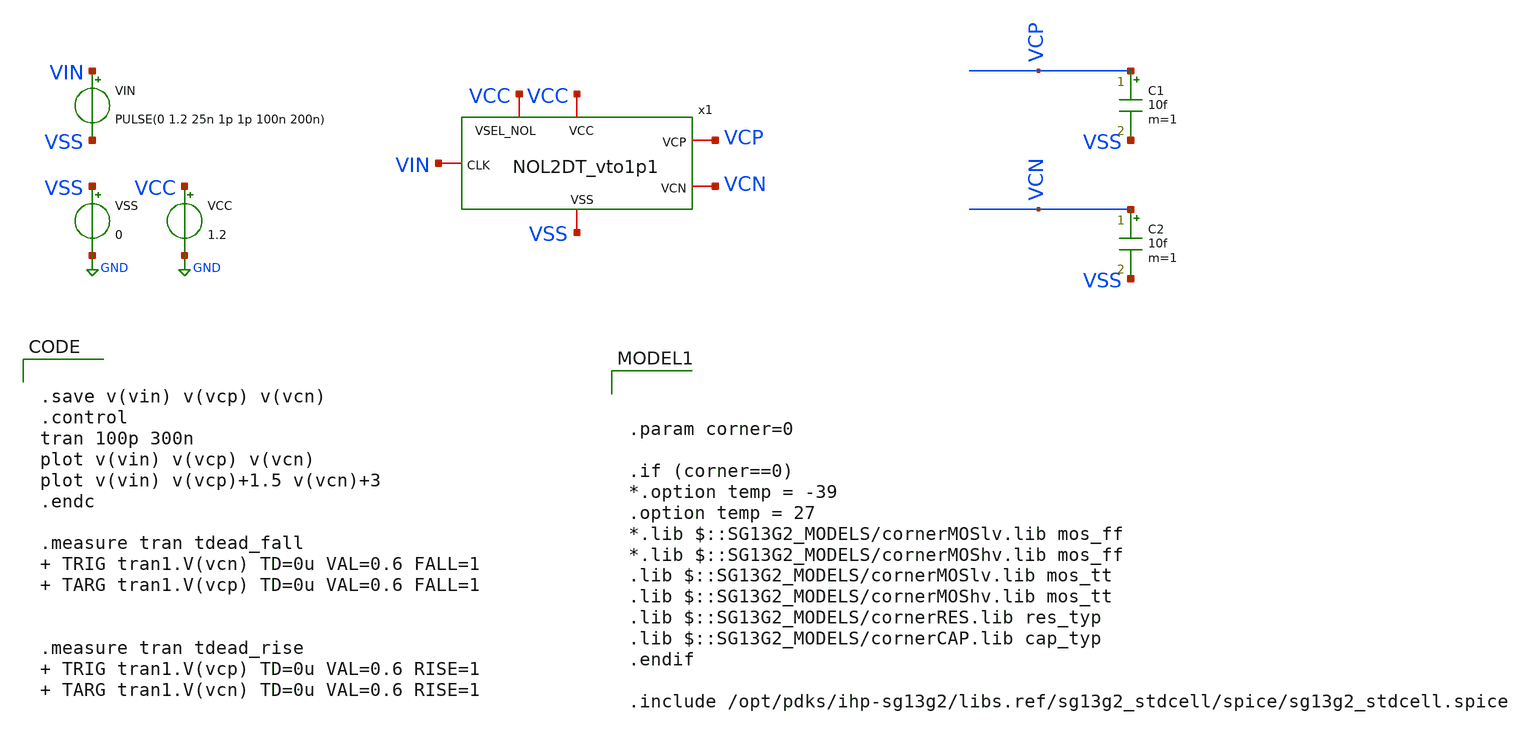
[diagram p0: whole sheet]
** sch_path: AC3E_USM_TDBUCK/design_data/xschem/NOL/tb_NOL2DT_vto1p1.sch
* IHP-GmbH/IHP-Open-PDK/ihp-sg13g2/libs.tech/xschem/sg13g2_stdcells/sg13g2_inv_2.sch:
* Copyright 2023 IHP PDK Authors
* Licensed under the Apache License, Version 2.0 (the "License");
**.subckt tb_NOL2DT_vto1p1
VCC VCC GND 1.2
VSS VSS GND 0
VIN VIN VSS PULSE(0 1.2 25n 1p 1p 100n 200n)
C1 VCP VSS 10f m=1
C2 VCN VSS 10f m=1
x1 VCC VSS VCP VIN VCN VCC NOL2DT_vto1p1
**** begin user architecture code


.save v(vin) v(vcp) v(vcn)
.control
tran 100p 300n
plot v(vin) v(vcp) v(vcn)
plot v(vin) v(vcp)+1.5 v(vcn)+3
.endc

.measure tran tdead_fall  TRIG tran1.V(vcn) TD=0u VAL=0.6 FALL=1  TARG tran1.V(vcp) TD=0u VAL=0.6
+ FALL=1


.measure tran tdead_rise  TRIG tran1.V(vcp) TD=0u VAL=0.6 RISE=1  TARG tran1.V(vcn) TD=0u VAL=0.6
+ RISE=1






.param corner=0

.if (corner==0)
*.option temp = -39
.option temp = 27
*.lib $::SG13G2_MODELS/cornerMOSlv.lib mos_ff
*.lib $::SG13G2_MODELS/cornerMOShv.lib mos_ff
.lib $::SG13G2_MODELS/cornerMOSlv.lib mos_tt
.lib $::SG13G2_MODELS/cornerMOShv.lib mos_tt
.lib $::SG13G2_MODELS/cornerRES.lib res_typ
.lib $::SG13G2_MODELS/cornerCAP.lib cap_typ
.endif

.include /opt/pdks/ihp-sg13g2/libs.ref/sg13g2_stdcell/spice/sg13g2_stdcell.spice

**** end user architecture code
**.ends

* expanding   symbol:  ../NOL/NOL2DT_vto1p1.sym # of pins=6
** sym_path: AC3E_USM_TDBUCK/design_data/xschem/NOL/NOL2DT_vto1p1.sym
** sch_path: AC3E_USM_TDBUCK/design_data/xschem/NOL/NOL2DT_vto1p1.sch
.subckt NOL2DT_vto1p1 VCC VSS VCP CLK VCN VSEL_NOL
*.iopin CLK
*.iopin VCP
*.iopin VCN
*.iopin VCC
*.iopin VSS
*.iopin VSEL_NOL
x5 A1 CLK VCC VSS sg13g2_inv_1
x3 C1 A1 B1 VCC VSS sg13g2_nor2_1
x1 C2 B2 CLK VCC VSS sg13g2_nor2_1
x2 net1 B1 VCC VSS sg13g2_inv_1
x6 net2 B2 VCC VSS sg13g2_inv_2
x7 net3 net1 VCC VSS sg13g2_inv_2
x8 VCN net2 VCC VSS sg13g2_inv_4
x9 VCP net3 VCC VSS sg13g2_inv_4
x10 VCC VSS C1 net9 large_delay_vto1p1
x4 VCC VSS C2 net7 large_delay_vto1p1
x11 B2 net9 net8 VSEL_NOL VCC VSS sg13g2_mux2_2
x12 VCC VSS net4 net8 large_delay_vto1p1
x13 VCC VSS C1 net4 large_delay_vto1p1
x14 B1 net7 net6 VSEL_NOL VCC VSS sg13g2_mux2_2
x15 VCC VSS net5 net6 large_delay_vto1p1
x16 VCC VSS C2 net5 large_delay_vto1p1
.ends


* expanding   symbol:  sg13g2_stdcells/sg13g2_inv_1.sym # of pins=2
** sym_path: sg13g2_stdcells/sg13g2_inv_1.sym
** sch_path: sg13g2_stdcells/sg13g2_inv_1.sch
.subckt sg13g2_inv_1 Y A VDD VSS
*.opin Y
*.ipin A
*.iopin VDD
*.iopin VSS
XM1 Y A VSS VSS sg13_lv_nmos w=740.00n l=130.00n ng=1 m=1 mm_ok=1
XM2 Y A VDD VDD sg13_lv_pmos w=1.12u l=130.00n ng=1 m=1 mm_ok=1
.ends


* expanding   symbol:  sg13g2_stdcells/sg13g2_nor2_1.sym # of pins=3
** sym_path: sg13g2_stdcells/sg13g2_nor2_1.sym
** sch_path: sg13g2_stdcells/sg13g2_nor2_1.sch
.subckt sg13g2_nor2_1 Y A B VDD VSS
*.opin Y
*.ipin B
*.ipin A
*.iopin VDD
*.iopin VSS
XM1 Y A VSS VSS sg13_lv_nmos w=740.00n l=130.00n ng=1 m=1 mm_ok=1
XM2 Y B VSS VSS sg13_lv_nmos w=740.00n l=130.00n ng=1 m=1 mm_ok=1
XM3 net1 A VDD VDD sg13_lv_pmos w=1.12u l=130.00n ng=1 m=1 mm_ok=1
XM4 Y B net1 VDD sg13_lv_pmos w=1.12u l=130.00n ng=1 m=1 mm_ok=1
.ends


* expanding   symbol:  sg13g2_stdcells/sg13g2_inv_2.sym # of pins=2
** sym_path: sg13g2_stdcells/sg13g2_inv_2.sym
** sch_path: sg13g2_stdcells/sg13g2_inv_2.sch
.subckt sg13g2_inv_2 Y A VDD VSS
*.opin Y
*.ipin A
*.iopin VDD
*.iopin VSS
XM1 Y A VSS VSS sg13_lv_nmos w=1.48u l=130.00n ng=2 m=1 mm_ok=1
XM2 Y A VDD VDD sg13_lv_pmos w=2.24u l=130.00n ng=2 m=1 mm_ok=1
.ends


* expanding   symbol:  sg13g2_stdcells/sg13g2_inv_4.sym # of pins=2
** sym_path: sg13g2_stdcells/sg13g2_inv_4.sym
** sch_path: sg13g2_stdcells/sg13g2_inv_4.sch
.subckt sg13g2_inv_4 Y A VDD VSS
*.ipin A
*.opin Y
*.iopin VDD
*.iopin VSS
XM1 Y A VSS VSS sg13_lv_nmos w=2.96u l=130.00n ng=4 m=1 mm_ok=1
XM2 Y A VDD VDD sg13_lv_pmos w=4.48u l=130.00n ng=4 m=1 mm_ok=1
.ends


* expanding   symbol:  ../large_delay/large_delay_vto1p1.sym # of pins=4
** sym_path: ../large_delay/large_delay_vto1p1.sym
** sch_path: ../large_delay/large_delay_vto1p1.sch
.subckt large_delay_vto1p1 VCC VSS VIN VOUT
*.iopin VIN
*.iopin VOUT
*.iopin VCC
*.iopin VSS
x1[0] n2 VIN VCC VSS sg13g2_dlygate4sd3_1
x1[1] n3 n2 VCC VSS sg13g2_dlygate4sd3_1
x1[2] n4 n3 VCC VSS sg13g2_dlygate4sd3_1
x1[3] n5 n4 VCC VSS sg13g2_dlygate4sd3_1
x1[4] VOUT n5 VCC VSS sg13g2_dlygate4sd3_1
.ends


* expanding   symbol:  sg13g2_stdcells/sg13g2_mux2_2.sym # of pins=4
** sym_path: sg13g2_stdcells/sg13g2_mux2_2.sym
** sch_path: sg13g2_stdcells/sg13g2_mux2_2.sch
.subckt sg13g2_mux2_2 X A0 A1 S VDD VSS
*.ipin S
*.ipin A0
*.ipin A1
*.opin X
*.iopin VDD
*.iopin VSS
XM1 Sb S VSS VSS sg13_lv_nmos w=550.00n l=130.00n ng=1 m=1 mm_ok=1
XM2 net1 A0 net5 VSS sg13_lv_nmos w=740.00n l=130.00n ng=1 m=1 mm_ok=1
XM3 net5 Sb VSS VSS sg13_lv_nmos w=740.00n l=130.00n ng=1 m=1 mm_ok=1
XM4 net1 A1 net4 VSS sg13_lv_nmos w=740.00n l=130.00n ng=1 m=1 mm_ok=1
XM5 net4 S VSS VSS sg13_lv_nmos w=740.00n l=130.00n ng=1 m=1 mm_ok=1
XM6 X net1 VSS VSS sg13_lv_nmos w=1.48u l=130.00n ng=2 m=1 mm_ok=1
XM7 Sb S VDD VDD sg13_lv_pmos w=840.00n l=130.00n ng=1 m=1 mm_ok=1
XM8 net2 S VDD VDD sg13_lv_pmos w=1.000u l=130.00n ng=1 m=1 mm_ok=1
XM9 net1 A0 net2 VDD sg13_lv_pmos w=1.000u l=130.00n ng=1 m=1 mm_ok=1
XM10 net3 Sb VDD VDD sg13_lv_pmos w=1.000u l=130.00n ng=1 m=1 mm_ok=1
XM11 net1 A1 net3 VDD sg13_lv_pmos w=1.000u l=130.00n ng=1 m=1 mm_ok=1
XM12 X net1 VDD VDD sg13_lv_pmos w=2.24u l=130.00n ng=2 m=1 mm_ok=1
.ends


* expanding   symbol:  sg13g2_stdcells/sg13g2_dlygate4sd3_1.sym # of pins=2
** sym_path: sg13g2_stdcells/sg13g2_dlygate4sd3_1.sym
** sch_path: sg13g2_stdcells/sg13g2_dlygate4sd3_1.sch
.subckt sg13g2_dlygate4sd3_1 X A VDD VSS
*.ipin A
*.opin X
*.iopin VDD
*.iopin VSS
XM1 net3 A VSS VSS sg13_lv_nmos w=420.00n l=130.00n ng=1 m=1 mm_ok=1
XM2 net1 net3 VSS VSS sg13_lv_nmos w=420.00n l=500.0n ng=1 m=1 mm_ok=1
XM3 net2 net1 VSS VSS sg13_lv_nmos w=420.00n l=500.0n ng=1 m=1 mm_ok=1
XM4 X net2 VSS VSS sg13_lv_nmos w=740.00n l=130.00n ng=1 m=1 mm_ok=1
XM5 net3 A VDD VDD sg13_lv_pmos w=420.00n l=130.00n ng=1 m=1 mm_ok=1
XM6 net1 net3 VDD VDD sg13_lv_pmos w=1.000u l=500.0n ng=1 m=1 mm_ok=1
XM7 net2 net1 VDD VDD sg13_lv_pmos w=1.000u l=500.0n ng=1 m=1 mm_ok=1
XM8 X net2 VDD VDD sg13_lv_pmos w=1.12u l=130.00n ng=1 m=1 mm_ok=1
.ends

.GLOBAL GND
.end
